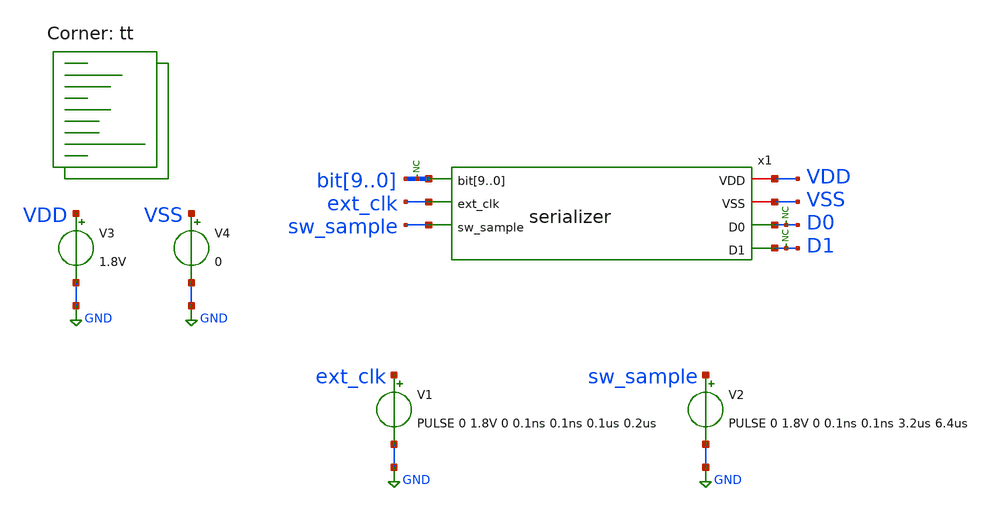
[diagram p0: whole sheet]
** sch_path: xschem/tests/serializer/serializer_test.sch
**.subckt serializer_test
V3 VDD GND 1.8V
V4 VSS GND 0
x1 VDD bit9 bit8 bit7 bit6 bit5 bit4 bit3 bit2 bit1 bit0 VSS ext_clk sw_sample D0 D1 serializer
V1 ext_clk GND PULSE 0 1.8V 0 0.1ns 0.1ns 0.1us 0.2us
V2 sw_sample GND PULSE 0 1.8V 0 0.1ns 0.1ns 3.2us 6.4us
* noconn bit[9..0]
* noconn D1
* noconn D0
**** begin user architecture code
 *.lib $::SKYWATER_MODELS/sky130.lib.spice tt
.include $::SKYWATER_STDCELLS/sky130_fd_sc_hd.spice


.options acct list
.temp 25

vbit0 bit0 gnd 1.8V
vbit1 bit1 gnd 1.8V
vbit2 bit2 gnd 0
vbit3 bit3 gnd 0
vbit4 bit4 gnd 1.8V
vbit5 bit5 gnd 1.8V
vbit6 bit6 gnd 0
vbit7 bit7 gnd 0
vbit8 bit8 gnd 1.8V
vbit9 bit9 gnd 1.8V

.control
tran 1n 13u
plot sw_sample-2 d0 d1+2 ext_clk+4
write serializer_test.raw
.endc


.lib $::SKYWATER_MODELS/sky130.lib.spice tt
**** end user architecture code
**.ends

* expanding   symbol:  src/serializer/serializer.sym # of pins=7
** sym_path: xschem/src/serializer/serializer.sym
** sch_path: xschem/src/serializer/serializer.sch
.subckt serializer VDD bit9 bit8 bit7 bit6 bit5 bit4 bit3 bit2 bit1 bit0 VSS ext_clk sw_sample D0 D1
*.ipin bit9,bit8,bit7,bit6,bit5,bit4,bit3,bit2,bit1,bit0
*.iopin VDD
*.opin D0
*.iopin VSS
*.opin D1
*.ipin ext_clk
*.ipin sw_sample
x1 clk net3 VSS VSS VDD VDD net2 sky130_fd_sc_hd__dfxtp_1
x2 clk net1 VSS VSS VDD VDD net7 sky130_fd_sc_hd__dfxtp_1
x4 VSS bit9 sel VSS VSS VDD VDD net3 sky130_fd_sc_hd__mux2_1
x5 clk net6 VSS VSS VDD VDD net5 sky130_fd_sc_hd__dfxtp_1
x6 clk net4 VSS VSS VDD VDD net9 sky130_fd_sc_hd__dfxtp_1
x9 clk net8 VSS VSS VDD VDD D1 sky130_fd_sc_hd__dfxtp_1
x10 clk net12 VSS VSS VDD VDD net11 sky130_fd_sc_hd__dfxtp_1
x11 clk net10 VSS VSS VDD VDD net16 sky130_fd_sc_hd__dfxtp_1
x15 clk net15 VSS VSS VDD VDD net14 sky130_fd_sc_hd__dfxtp_1
x16 clk net13 VSS VSS VDD VDD net18 sky130_fd_sc_hd__dfxtp_1
x19 clk net17 VSS VSS VDD VDD D0 sky130_fd_sc_hd__dfxtp_1
x21 net19 net20 VSS VSS VDD VDD net21 net20 sky130_fd_sc_hd__dfxbp_1
x22 clk VDD reset_cycle VSS VSS VDD VDD net22 sky130_fd_sc_hd__dfrtp_1
x23 clk net22 reset_cycle VSS VSS VDD VDD net26 sky130_fd_sc_hd__dfrtp_1
x24 net22 VSS VSS VDD VDD net23 sky130_fd_sc_hd__buf_2
x25 net23 VSS VSS VDD VDD net24 sky130_fd_sc_hd__buf_4
x26 net24 VSS VSS VDD VDD net25 sky130_fd_sc_hd__buf_8
x27 net25 VSS VSS VDD VDD sel sky130_fd_sc_hd__bufinv_16
x28 clk net26 reset_cycle VSS VSS VDD VDD net27 sky130_fd_sc_hd__dfrtp_1
x29 clk net27 reset_cycle VSS VSS VDD VDD net28 sky130_fd_sc_hd__dfrtp_1
x30 clk net28 reset_cycle VSS VSS VDD VDD net29 sky130_fd_sc_hd__dfrtp_1
x31 clk net29 reset_cycle VSS VSS VDD VDD end sky130_fd_sc_hd__dfrtp_1
x32 end VSS VSS VDD VDD net30 sky130_fd_sc_hd__clkdlybuf4s50_1
x33 net30 VSS VSS VDD VDD net31 sky130_fd_sc_hd__clkdlybuf4s50_1
x34 net31 VSS VSS VDD VDD net32 sky130_fd_sc_hd__clkdlybuf4s50_1
x35 net32 VSS VSS VDD VDD net33 sky130_fd_sc_hd__clkdlybuf4s50_1
x36 net33 VSS VSS VDD VDD net34 sky130_fd_sc_hd__clkdlybuf4s50_1
x38 net35 VSS VSS VDD VDD net36 sky130_fd_sc_hd__buf_4
x39 net36 VSS VSS VDD VDD reset_cycle sky130_fd_sc_hd__buf_8
x40 net37 VSS VSS VDD VDD net35 sky130_fd_sc_hd__buf_2
x41 net21 VSS VSS VDD VDD net38 sky130_fd_sc_hd__buf_2
x42 net38 VSS VSS VDD VDD net39 sky130_fd_sc_hd__buf_4
x43 net39 VSS VSS VDD VDD clk sky130_fd_sc_hd__buf_8
x44 net40 ext_clk VSS VSS VDD VDD net19 sky130_fd_sc_hd__and2_0
x45 sw_sample VSS VSS VDD VDD net40 sky130_fd_sc_hd__inv_1
x3 VSS bit8 sel VSS VSS VDD VDD net12 sky130_fd_sc_hd__mux2_1
x7 net2 bit7 sel VSS VSS VDD VDD net1 sky130_fd_sc_hd__mux2_1
x8 net7 bit5 sel VSS VSS VDD VDD net6 sky130_fd_sc_hd__mux2_1
x12 net11 bit6 sel VSS VSS VDD VDD net10 sky130_fd_sc_hd__mux2_1
x13 net16 bit4 sel VSS VSS VDD VDD net15 sky130_fd_sc_hd__mux2_1
x14 net5 bit3 sel VSS VSS VDD VDD net4 sky130_fd_sc_hd__mux2_1
x17 net14 bit2 sel VSS VSS VDD VDD net13 sky130_fd_sc_hd__mux2_1
x18 net9 bit1 sel VSS VSS VDD VDD net8 sky130_fd_sc_hd__mux2_1
x20 net18 bit0 sel VSS VSS VDD VDD net17 sky130_fd_sc_hd__mux2_1
x37 net34 end VSS VSS VDD VDD net37 sky130_fd_sc_hd__xnor2_1
.ends

.GLOBAL GND
.end
